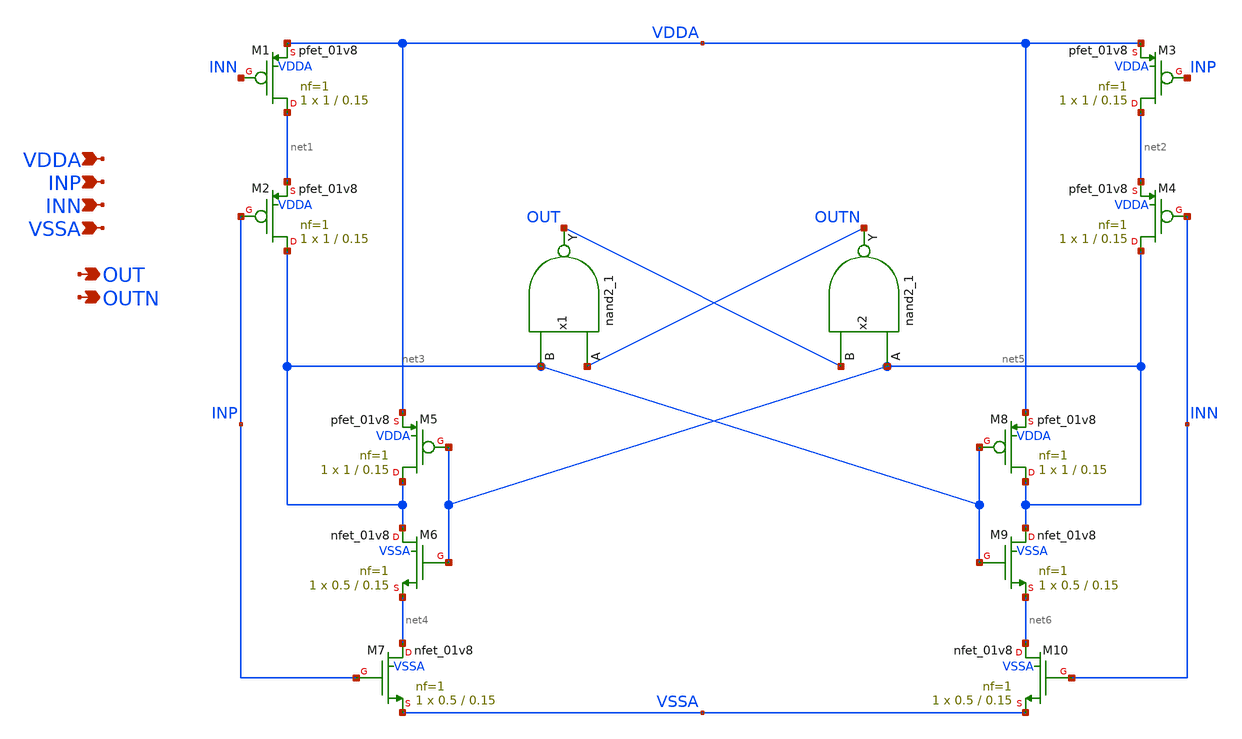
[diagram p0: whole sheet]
** sch_path: xschem/phase_detector.sch
**.subckt phase_detector VDDA INP INN VSSA OUT OUTN
*.ipin VDDA
*.ipin INP
*.ipin INN
*.ipin VSSA
*.opin OUT
*.opin OUTN
x1 OUTN net3 VSSA VSSA VDDA VDDA OUT sky130_fd_sc_hd__nand2_1
x2 net5 OUT VSSA VSSA VDDA VDDA OUTN sky130_fd_sc_hd__nand2_1
XM1 net1 INN VDDA VDDA sky130_fd_pr__pfet_01v8 L=0.15 W=1 nf=1 ad='int((nf+1)/2) * W/nf * 0.29' as='int((nf+2)/2) * W/nf * 0.29'
+ pd='2*int((nf+1)/2) * (W/nf + 0.29)' ps='2*int((nf+2)/2) * (W/nf + 0.29)' nrd='0.29 / W' nrs='0.29 / W'
+ sa=0 sb=0 sd=0 mult=1 m=1
XM2 net3 INP net1 VDDA sky130_fd_pr__pfet_01v8 L=0.15 W=1 nf=1 ad='int((nf+1)/2) * W/nf * 0.29' as='int((nf+2)/2) * W/nf * 0.29'
+ pd='2*int((nf+1)/2) * (W/nf + 0.29)' ps='2*int((nf+2)/2) * (W/nf + 0.29)' nrd='0.29 / W' nrs='0.29 / W'
+ sa=0 sb=0 sd=0 mult=1 m=1
XM3 net2 INP VDDA VDDA sky130_fd_pr__pfet_01v8 L=0.15 W=1 nf=1 ad='int((nf+1)/2) * W/nf * 0.29' as='int((nf+2)/2) * W/nf * 0.29'
+ pd='2*int((nf+1)/2) * (W/nf + 0.29)' ps='2*int((nf+2)/2) * (W/nf + 0.29)' nrd='0.29 / W' nrs='0.29 / W'
+ sa=0 sb=0 sd=0 mult=1 m=1
XM4 net5 INN net2 VDDA sky130_fd_pr__pfet_01v8 L=0.15 W=1 nf=1 ad='int((nf+1)/2) * W/nf * 0.29' as='int((nf+2)/2) * W/nf * 0.29'
+ pd='2*int((nf+1)/2) * (W/nf + 0.29)' ps='2*int((nf+2)/2) * (W/nf + 0.29)' nrd='0.29 / W' nrs='0.29 / W'
+ sa=0 sb=0 sd=0 mult=1 m=1
XM5 net3 net5 VDDA VDDA sky130_fd_pr__pfet_01v8 L=0.15 W=1 nf=1 ad='int((nf+1)/2) * W/nf * 0.29' as='int((nf+2)/2) * W/nf * 0.29'
+ pd='2*int((nf+1)/2) * (W/nf + 0.29)' ps='2*int((nf+2)/2) * (W/nf + 0.29)' nrd='0.29 / W' nrs='0.29 / W'
+ sa=0 sb=0 sd=0 mult=1 m=1
XM6 net3 net5 net4 VSSA sky130_fd_pr__nfet_01v8 L=0.15 W=0.5 nf=1 ad='int((nf+1)/2) * W/nf * 0.29' as='int((nf+2)/2) * W/nf * 0.29'
+ pd='2*int((nf+1)/2) * (W/nf + 0.29)' ps='2*int((nf+2)/2) * (W/nf + 0.29)' nrd='0.29 / W' nrs='0.29 / W'
+ sa=0 sb=0 sd=0 mult=1 m=1
XM7 net4 INP VSSA VSSA sky130_fd_pr__nfet_01v8 L=0.15 W=0.5 nf=1 ad='int((nf+1)/2) * W/nf * 0.29' as='int((nf+2)/2) * W/nf * 0.29'
+ pd='2*int((nf+1)/2) * (W/nf + 0.29)' ps='2*int((nf+2)/2) * (W/nf + 0.29)' nrd='0.29 / W' nrs='0.29 / W'
+ sa=0 sb=0 sd=0 mult=1 m=1
XM8 net5 net3 VDDA VDDA sky130_fd_pr__pfet_01v8 L=0.15 W=1 nf=1 ad='int((nf+1)/2) * W/nf * 0.29' as='int((nf+2)/2) * W/nf * 0.29'
+ pd='2*int((nf+1)/2) * (W/nf + 0.29)' ps='2*int((nf+2)/2) * (W/nf + 0.29)' nrd='0.29 / W' nrs='0.29 / W'
+ sa=0 sb=0 sd=0 mult=1 m=1
XM9 net5 net3 net6 VSSA sky130_fd_pr__nfet_01v8 L=0.15 W=0.5 nf=1 ad='int((nf+1)/2) * W/nf * 0.29' as='int((nf+2)/2) * W/nf * 0.29'
+ pd='2*int((nf+1)/2) * (W/nf + 0.29)' ps='2*int((nf+2)/2) * (W/nf + 0.29)' nrd='0.29 / W' nrs='0.29 / W'
+ sa=0 sb=0 sd=0 mult=1 m=1
XM10 net6 INN VSSA VSSA sky130_fd_pr__nfet_01v8 L=0.15 W=0.5 nf=1 ad='int((nf+1)/2) * W/nf * 0.29' as='int((nf+2)/2) * W/nf * 0.29'
+ pd='2*int((nf+1)/2) * (W/nf + 0.29)' ps='2*int((nf+2)/2) * (W/nf + 0.29)' nrd='0.29 / W' nrs='0.29 / W'
+ sa=0 sb=0 sd=0 mult=1 m=1
**.ends
.end
